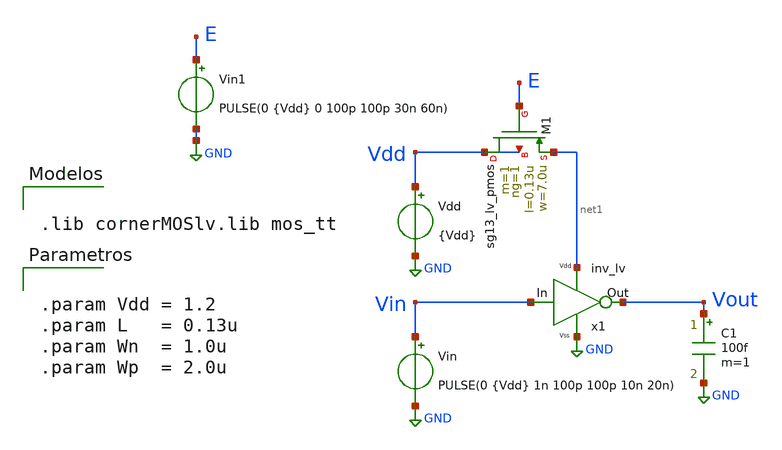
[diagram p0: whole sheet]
** sch_path: Taller1/Resuelto/Power_reduction_solved.sch
**.subckt Power_reduction_solved
C1 Vout GND 100f m=1
Vin Vin GND PULSE(0 {Vdd} 1n 100p 100p 10n 20n)
Vdd Vdd GND {Vdd}
x1 Vin Vout net1 GND inv_lv
Vin1 E GND PULSE(0 {Vdd} 0 100p 100p 30n 60n)
XM1 Vdd E net1 Vdd sg13_lv_pmos w=7.0u l=0.13u ng=1 m=1 mm_ok=1
**** begin user architecture code


.lib cornerMOSlv.lib mos_tt




.param Vdd = 1.2
.param L   = 0.13u
.param Wn  = 1.0u
.param Wp  = 2.0u




.control

tran 100p 100n
plot v(Vin)
plot v(vout) v(E)

meas tran fall_time Trig  v(Vin) VAL=0.6 RISE=1 TARG v(Vout) VAL=0.6 FALL=1
meas tran rise_time Trig  v(Vin) VAL=0.6 FALL=1 TARG v(Vout) VAL=0.6 RISE=1

let time_diff = abs(fall_time - rise_time)
let prop_time = (fall_time + rise_time)/2

print time_diff
print prop_time
.endc


**** end user architecture code
**.ends

* expanding   symbol:  ../Insumos/inv_lv.sym # of pins=4
** sym_path: ../Insumos/inv_lv.sym
** sch_path: ../Insumos/inv_lv.sch
.subckt inv_lv Vin Vout Vdd Vss
*.ipin Vdd
*.ipin Vss
*.ipin Vin
*.opin Vout
XM1 Vss Vin Vout Vss sg13_lv_nmos w={Wn} l={L} ng=1 m=1 mm_ok=1
XM2 Vout Vin Vdd Vdd sg13_lv_pmos w={Wp} l={L} ng=1 m=1 mm_ok=1
.ends

.GLOBAL GND
.end
